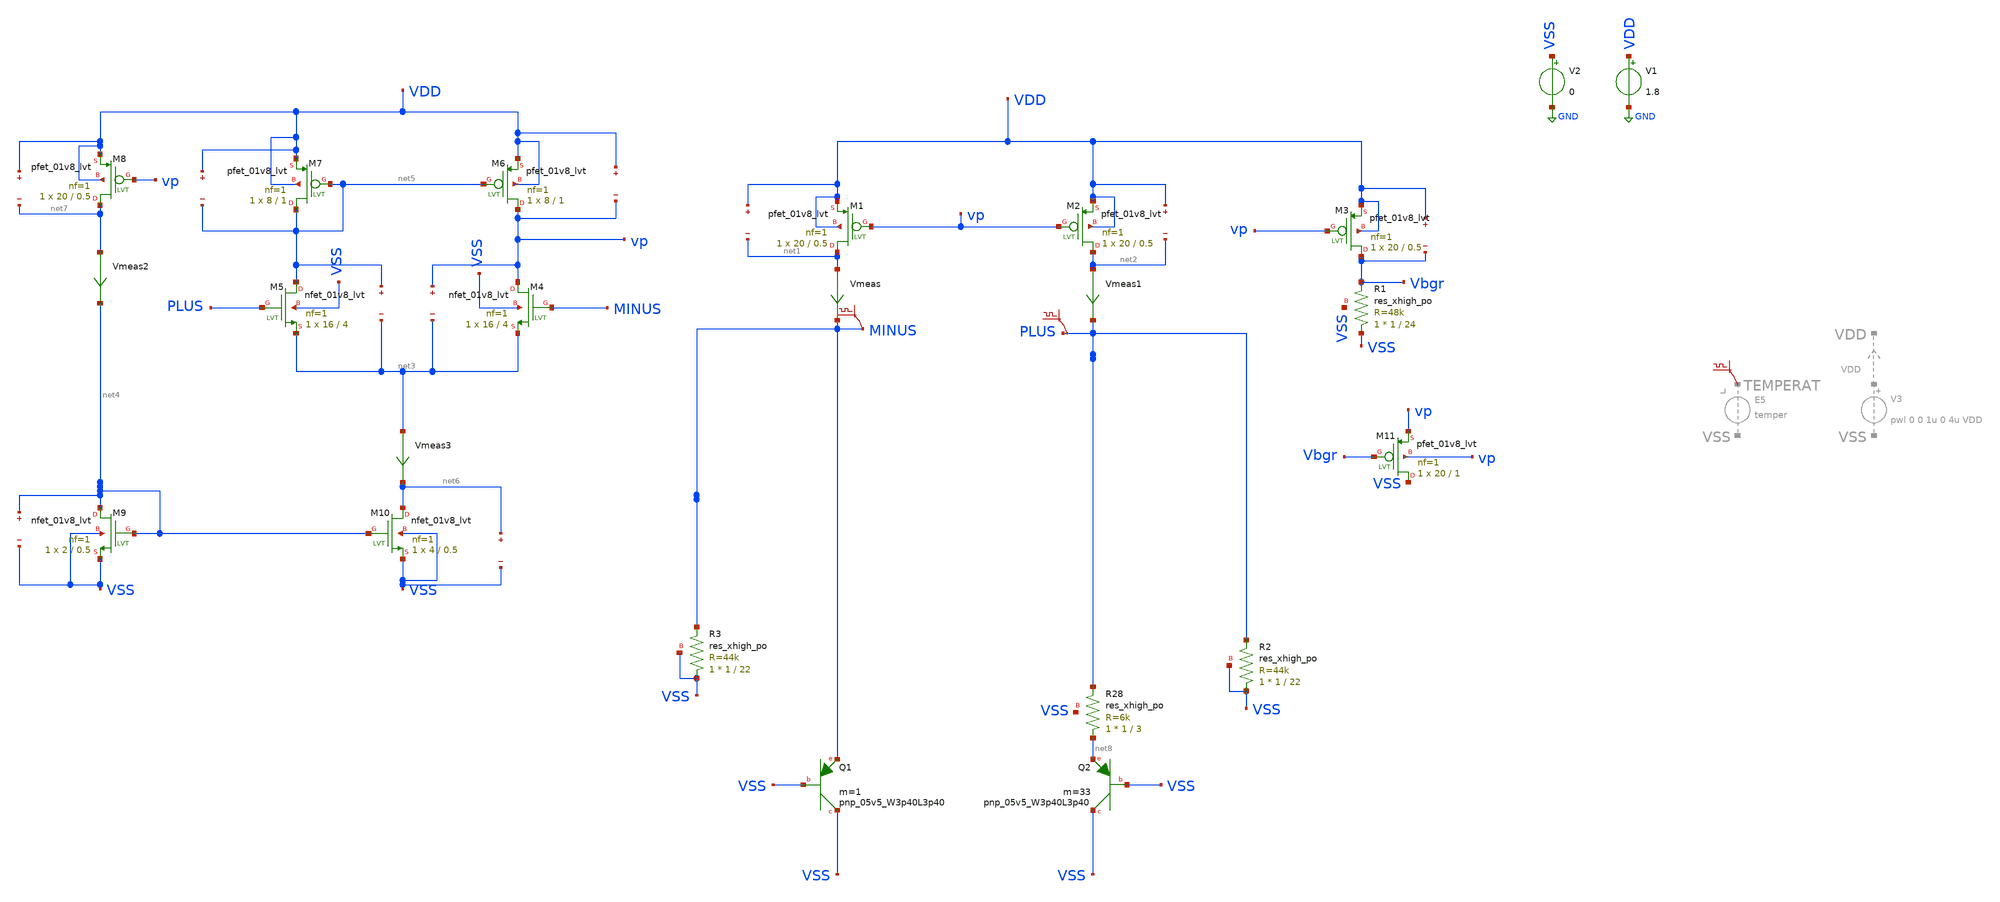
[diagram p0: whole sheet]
** sch_path: xschem/BGRwOpampRes.sch
**.subckt BGRwOpampRes
XQ1 VSS VSS MINUS sky130_fd_pr__pnp_05v5_W3p40L3p40 m=1
XQ2 VSS VSS net8 sky130_fd_pr__pnp_05v5_W3p40L3p40 m=33
XM1 net1 vp VDD VDD sky130_fd_pr__pfet_01v8_lvt L=0.5 W=20 nf=1 ad='int((nf+1)/2) * W/nf * 0.29' as='int((nf+2)/2) * W/nf * 0.29'
+ pd='2*int((nf+1)/2) * (W/nf + 0.29)' ps='2*int((nf+2)/2) * (W/nf + 0.29)' nrd='0.29 / W' nrs='0.29 / W'
+ sa=0 sb=0 sd=0 mult=1 m=1
XM2 net2 vp VDD VDD sky130_fd_pr__pfet_01v8_lvt L=0.5 W=20 nf=1 ad='int((nf+1)/2) * W/nf * 0.29' as='int((nf+2)/2) * W/nf * 0.29'
+ pd='2*int((nf+1)/2) * (W/nf + 0.29)' ps='2*int((nf+2)/2) * (W/nf + 0.29)' nrd='0.29 / W' nrs='0.29 / W'
+ sa=0 sb=0 sd=0 mult=1 m=1
XM3 Vbgr vp VDD VDD sky130_fd_pr__pfet_01v8_lvt L=0.5 W=20 nf=1 ad='int((nf+1)/2) * W/nf * 0.29' as='int((nf+2)/2) * W/nf * 0.29'
+ pd='2*int((nf+1)/2) * (W/nf + 0.29)' ps='2*int((nf+2)/2) * (W/nf + 0.29)' nrd='0.29 / W' nrs='0.29 / W'
+ sa=0 sb=0 sd=0 mult=1 m=1
V1 VDD GND 1.8
V2 VSS GND 0
Vmeas net1 MINUS 0
.save i(vmeas)
Vmeas1 net2 PLUS 0
.save i(vmeas1)
.save v(vdd)
.save v(net1)
.save v(vdd)
.save v(net2)
.save v(vdd)
.save v(vbgr)
XM4 vp MINUS net3 VSS sky130_fd_pr__nfet_01v8_lvt L=4 W=16 nf=1 ad='int((nf+1)/2) * W/nf * 0.29' as='int((nf+2)/2) * W/nf * 0.29'
+ pd='2*int((nf+1)/2) * (W/nf + 0.29)' ps='2*int((nf+2)/2) * (W/nf + 0.29)' nrd='0.29 / W' nrs='0.29 / W'
+ sa=0 sb=0 sd=0 mult=1 m=1
XM5 net5 PLUS net3 VSS sky130_fd_pr__nfet_01v8_lvt L=4 W=16 nf=1 ad='int((nf+1)/2) * W/nf * 0.29' as='int((nf+2)/2) * W/nf * 0.29'
+ pd='2*int((nf+1)/2) * (W/nf + 0.29)' ps='2*int((nf+2)/2) * (W/nf + 0.29)' nrd='0.29 / W' nrs='0.29 / W'
+ sa=0 sb=0 sd=0 mult=1 m=1
XM6 vp net5 VDD VDD sky130_fd_pr__pfet_01v8_lvt L=1 W=8 nf=1 ad='int((nf+1)/2) * W/nf * 0.29' as='int((nf+2)/2) * W/nf * 0.29'
+ pd='2*int((nf+1)/2) * (W/nf + 0.29)' ps='2*int((nf+2)/2) * (W/nf + 0.29)' nrd='0.29 / W' nrs='0.29 / W'
+ sa=0 sb=0 sd=0 mult=1 m=1
.save v(vp)
.save v(net3)
.save v(net5)
.save v(net3)
XM10 net6 net4 VSS VSS sky130_fd_pr__nfet_01v8_lvt L=0.5 W=4 nf=1 ad='int((nf+1)/2) * W/nf * 0.29' as='int((nf+2)/2) * W/nf * 0.29'
+ pd='2*int((nf+1)/2) * (W/nf + 0.29)' ps='2*int((nf+2)/2) * (W/nf + 0.29)' nrd='0.29 / W' nrs='0.29 / W'
+ sa=0 sb=0 sd=0 mult=1 m=1
XM9 net4 net4 VSS VSS sky130_fd_pr__nfet_01v8_lvt L=0.5 W=2 nf=1 ad='int((nf+1)/2) * W/nf * 0.29' as='int((nf+2)/2) * W/nf * 0.29'
+ pd='2*int((nf+1)/2) * (W/nf + 0.29)' ps='2*int((nf+2)/2) * (W/nf + 0.29)' nrd='0.29 / W' nrs='0.29 / W'
+ sa=0 sb=0 sd=0 mult=1 m=1
XM7 net5 net5 VDD VDD sky130_fd_pr__pfet_01v8_lvt L=1 W=8 nf=1 ad='int((nf+1)/2) * W/nf * 0.29' as='int((nf+2)/2) * W/nf * 0.29'
+ pd='2*int((nf+1)/2) * (W/nf + 0.29)' ps='2*int((nf+2)/2) * (W/nf + 0.29)' nrd='0.29 / W' nrs='0.29 / W'
+ sa=0 sb=0 sd=0 mult=1 m=1
.save v(vdd)
.save v(net5)
.save v(vdd)
.save v(vp)
.save v(net6)
.save v(vss)
.save v(net4)
.save v(vss)
Vmeas3 net3 net6 0
.save i(vmeas3)
XM8 net7 vp VDD VDD sky130_fd_pr__pfet_01v8_lvt L=0.5 W=20 nf=1 ad='int((nf+1)/2) * W/nf * 0.29' as='int((nf+2)/2) * W/nf * 0.29'
+ pd='2*int((nf+1)/2) * (W/nf + 0.29)' ps='2*int((nf+2)/2) * (W/nf + 0.29)' nrd='0.29 / W' nrs='0.29 / W'
+ sa=0 sb=0 sd=0 mult=1 m=1
Vmeas2 net7 net4 0
.save i(vmeas2)
.save v(vdd)
.save v(net7)
XR2 VSS PLUS VSS sky130_fd_pr__res_xhigh_po W=1 L=22 mult=1 m=1
XR3 VSS MINUS VSS sky130_fd_pr__res_xhigh_po W=1 L=22 mult=1 m=1
XM11 VSS Vbgr vp vp sky130_fd_pr__pfet_01v8_lvt L=1 W=20 nf=1 ad='int((nf+1)/2) * W/nf * 0.29' as='int((nf+2)/2) * W/nf * 0.29'
+ pd='2*int((nf+1)/2) * (W/nf + 0.29)' ps='2*int((nf+2)/2) * (W/nf + 0.29)' nrd='0.29 / W' nrs='0.29 / W'
+ sa=0 sb=0 sd=0 mult=1 m=1
.save v(minus)
.save v(plus)
XR28 net8 PLUS VSS sky130_fd_pr__res_xhigh_po W=1 L=3 mult=1 m=1
XR1 VSS Vbgr VSS sky130_fd_pr__res_xhigh_po W=1 L=24 mult=1 m=1
**** begin user architecture code

** opencircuitdesign pdks install
.lib $::SKYWATER_MODELS/sky130.lib.spice tt


**** end user architecture code
**.ends
.GLOBAL GND
**** begin user architecture code



.options savecurrents
.control


save @m.xm1.msky130_fd_pr__ppet_01v8_lvt[gm]
save @m.xm1.msky130_fd_pr__pfet_01v8_lvt[id]
save @m.xm1.msky130_fd_pr__pfet_01v8_lvt[vgs]
save @m.xm1.msky130_fd_pr__pfet_01v8_lvt[vds]
save @m.xm1.msky130_fd_pr__pfet_01v8_lvt[cgg]
save @m.xm1.msky130_fd_pr__pfet_01v8_lvt[vdsat]
save @m.xm1.msky130_fd_pr__pfet_01v8_lvt[vth]


save @m.xm2.msky130_fd_pr__pfet_01v8_lvt[gm]
save @m.xm2.msky130_fd_pr__pfet_01v8_lvt[id]
save @m.xm2.msky130_fd_pr__pfet_01v8_lvt[vgs]
save @m.xm2.msky130_fd_pr__pfet_01v8_lvt[vds]
save @m.xm2.msky130_fd_pr__pfet_01v8_lvt[cgg]
save @m.xm2.msky130_fd_pr__pfet_01v8_lvt[vdsat]
save @m.xm2.msky130_fd_pr__pfet_01v8_lvt[vth]


save @m.xm3.msky130_fd_pr__pfet_01v8_lvt[gm]
save @m.xm3.msky130_fd_pr__pfet_01v8_lvt[id]
save @m.xm3.msky130_fd_pr__pfet_01v8_lvt[vgs]
save @m.xm3.msky130_fd_pr__pfet_01v8_lvt[vds]
save @m.xm3.msky130_fd_pr__pfet_01v8_lvt[cgg]
save @m.xm3.msky130_fd_pr__pfet_01v8_lvt[vdsat]
save @m.xm3.msky130_fd_pr__pfet_01v8_lvt[vth]

save @q.xq1.qsky130_fd_pr__pnp_05v5_W3p40L3p40[vbe]
save @q.xq2.qsky130_fd_pr__pnp_05v5_W3p40L3p40[vbe]


save @m.xm6.msky130_fd_pr__pfet_01v8_lvt[gm]
save @m.xm6.msky130_fd_pr__pfet_01v8_lvt[id]
save @m.xm6.msky130_fd_pr__pfet_01v8_lvt[vgs]
save @m.xm6.msky130_fd_pr__pfet_01v8_lvt[vds]
save @m.xm6.msky130_fd_pr__pfet_01v8_lvt[cgg]
save @m.xm6.msky130_fd_pr__pfet_01v8_lvt[vdsat]
save @m.xm6.msky130_fd_pr__pfet_01v8_lvt[vth]

save @m.xm7.msky130_fd_pr__pfet_01v8_lvt[gm]
save @m.xm7.msky130_fd_pr__pfet_01v8_lvt[id]
save @m.xm7.msky130_fd_pr__pfet_01v8_lvt[vgs]
save @m.xm7.msky130_fd_pr__pfet_01v8_lvt[vds]
save @m.xm7.msky130_fd_pr__pfet_01v8_lvt[cgg]
save @m.xm7.msky130_fd_pr__pfet_01v8_lvt[vdsat]
save @m.xm7.msky130_fd_pr__pfet_01v8_lvt[vth]



save @m.xm8.msky130_fd_pr__pfet_01v8_lvt[gm]
save @m.xm8.msky130_fd_pr__pfet_01v8_lvt[id]
save @m.xm8.msky130_fd_pr__pfet_01v8_lvt[vgs]
save @m.xm8.msky130_fd_pr__pfet_01v8_lvt[vds]
save @m.xm8.msky130_fd_pr__pfet_01v8_lvt[cgg]
save @m.xm8.msky130_fd_pr__pfet_01v8_lvt[vdsat]
save @m.xm8.msky130_fd_pr__pfet_01v8_lvt[vth]


save @m.xm4.msky130_fd_pr__nfet_01v8_lvt[gm]
save @m.xm4.msky130_fd_pr__nfet_01v8_lvt[id]
save @m.xm4.msky130_fd_pr__nfet_01v8_lvt[vgs]
save @m.xm4.msky130_fd_pr__nfet_01v8_lvt[vds]
save @m.xm4.msky130_fd_pr__nfet_01v8_lvt[cgg]
save @m.xm4.msky130_fd_pr__nfet_01v8_lvt[vdsat]
save @m.xm4.msky130_fd_pr__nfet_01v8_lvt[vth]


save @m.xm5.msky130_fd_pr__nfet_01v8_lvt[gm]
save @m.xm5.msky130_fd_pr__nfet_01v8_lvt[id]
save @m.xm5.msky130_fd_pr__nfet_01v8_lvt[vgs]
save @m.xm5.msky130_fd_pr__nfet_01v8_lvt[vds]
save @m.xm5.msky130_fd_pr__nfet_01v8_lvt[cgg]
save @m.xm5.msky130_fd_pr__nfet_01v8_lvt[vdsat]
save @m.xm5.msky130_fd_pr__nfet_01v8_lvt[vth]



save @m.xm9.msky130_fd_pr__nfet_01v8_lvt[gm]
save @m.xm9.msky130_fd_pr__nfet_01v8_lvt[id]
save @m.xm9.msky130_fd_pr__nfet_01v8_lvt[vgs]
save @m.xm9.msky130_fd_pr__nfet_01v8_lvt[vds]
save @m.xm9.msky130_fd_pr__nfet_01v8_lvt[cgg]
save @m.xm9.msky130_fd_pr__nfet_01v8_lvt[vdsat]
save @m.xm9.msky130_fd_pr__nfet_01v8_lvt[vth]



save @m.xm10.msky130_fd_pr__nfet_01v8_lvt[gm]
save @m.xm10.msky130_fd_pr__nfet_01v8_lvt[id]
save @m.xm10.msky130_fd_pr__nfet_01v8_lvt[vgs]
save @m.xm10.msky130_fd_pr__nfet_01v8_lvt[vds]
save @m.xm10.msky130_fd_pr__nfet_01v8_lvt[cgg]
save @m.xm10.msky130_fd_pr__nfet_01v8_lvt[vdsat]
save @m.xm10.msky130_fd_pr__nfet_01v8_lvt[vth]


save @m.xm11.msky130_fd_pr__nfet_01v8_lvt[gm]
save @m.xm11.msky130_fd_pr__nfet_01v8_lvt[id]
save @m.xm11.msky130_fd_pr__nfet_01v8_lvt[vgs]
save @m.xm11.msky130_fd_pr__nfet_01v8_lvt[vds]
save @m.xm11.msky130_fd_pr__nfet_01v8_lvt[cgg]
save @m.xm11.msky130_fd_pr__nfet_01v8_lvt[vdsat]
save @m.xm11.msky130_fd_pr__nfet_01v8_lvt[vth]
save all
op
write BGRwOpampRes.raw
dc TEMP -40 125 10
plot Vbgr
*tran 20p 2u
*write BGRwOpampRes_startup.raw
.endc



**** end user architecture code
.end
